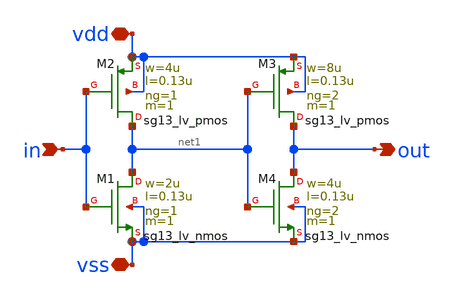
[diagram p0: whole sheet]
** sch_path: SSDOR_1.2V_v4/components/cgenerator/buff_ring_osc.sch
**.subckt buff_ring_osc in vdd vss out
*.ipin in
*.iopin vdd
*.iopin vss
*.opin out
XM1 net1 in vss vss sg13_lv_nmos w=2u l=0.13u ng=1 m=1 mm_ok=1
XM2 net1 in vdd vdd sg13_lv_pmos w=4u l=0.13u ng=1 m=1 mm_ok=1
XM3 out net1 vdd vdd sg13_lv_pmos w=8u l=0.13u ng=2 m=1 mm_ok=1
XM4 out net1 vss vss sg13_lv_nmos w=4u l=0.13u ng=2 m=1 mm_ok=1
**.ends
.end
